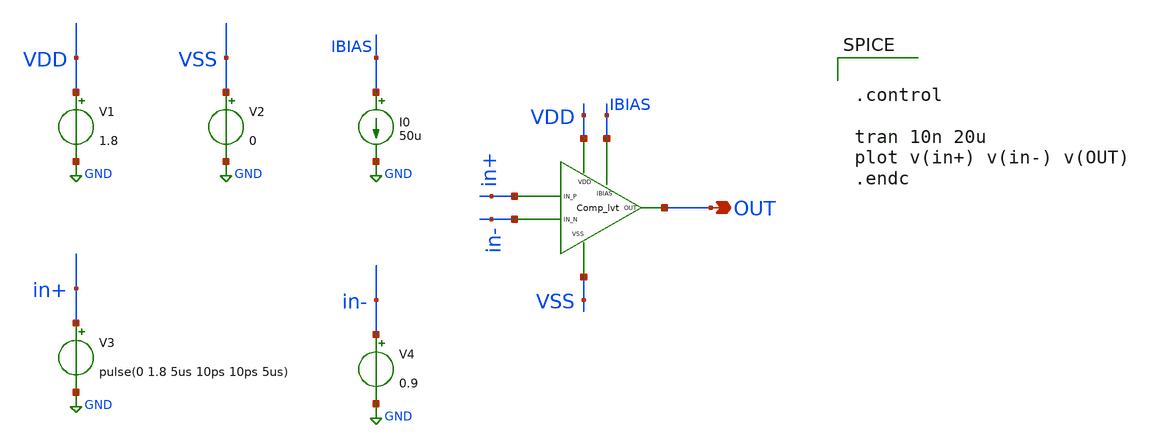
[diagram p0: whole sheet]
** sch_path: xschem/DC_DC_Converter_xschem/OTHERS/DC_DC_Converter_V7/Comparator/Comp_lvt_TB.sch
**.subckt Comp_lvt_TB OUT
*.opin OUT
XM1 IBIAS VDD in+ in- VSS OUT Comp_lvt
V1 VDD GND 1.8
V2 VSS GND 0
V3 in+ GND pulse(0 1.8 5us 10ps 10ps 5us)
V4 in- GND 0.9
I0 IBIAS GND 50u
**** begin user architecture code


.control

tran 10n 20u
plot v(in+) v(in-) v(OUT)
.endc



** opencircuitdesign pdks install
.lib $::SKYWATER_MODELS/sky130.lib.spice tt


**** end user architecture code
**.ends

* expanding   symbol:  DC_DC_Converter/Comparator/Comp_lvt.sym # of pins=6
** sym_path: xschem/DC_DC_Converter_xschem/OTHERS/DC_DC_Converter_V7/Comparator/Comp_lvt.sym
** sch_path: xschem/DC_DC_Converter_xschem/OTHERS/DC_DC_Converter_V7/Comparator/Comp_lvt.sch
.subckt Comp_lvt IBIAS VDD IN_P IN_N VSS OUT
*.iopin VSS
*.iopin VDD
*.iopin IN_P
*.iopin IN_N
*.iopin OUT
*.iopin IBIAS
XM16 2_P 1_N VDD VDD sky130_fd_pr__pfet_01v8_lvt L=0.5 W=3 nf=1 ad='int((nf+1)/2) * W/nf * 0.29' as='int((nf+2)/2) * W/nf * 0.29'
+ pd='2*int((nf+1)/2) * (W/nf + 0.29)' ps='2*int((nf+2)/2) * (W/nf + 0.29)' nrd='0.29 / W' nrs='0.29 / W'
+ sa=0 sb=0 sd=0 mult=1 m=1
XM4 1_N 1_N VDD VDD sky130_fd_pr__pfet_01v8_lvt L=0.5 W=3 nf=1 ad='int((nf+1)/2) * W/nf * 0.29' as='int((nf+2)/2) * W/nf * 0.29'
+ pd='2*int((nf+1)/2) * (W/nf + 0.29)' ps='2*int((nf+2)/2) * (W/nf + 0.29)' nrd='0.29 / W' nrs='0.29 / W'
+ sa=0 sb=0 sd=0 mult=1 m=1
XM5 1_N 1_P VDD VDD sky130_fd_pr__pfet_01v8_lvt L=0.5 W=3 nf=1 ad='int((nf+1)/2) * W/nf * 0.29' as='int((nf+2)/2) * W/nf * 0.29'
+ pd='2*int((nf+1)/2) * (W/nf + 0.29)' ps='2*int((nf+2)/2) * (W/nf + 0.29)' nrd='0.29 / W' nrs='0.29 / W'
+ sa=0 sb=0 sd=0 mult=1 m=1
XM3 1_P 1_N VDD VDD sky130_fd_pr__pfet_01v8_lvt L=0.5 W=3 nf=1 ad='int((nf+1)/2) * W/nf * 0.29' as='int((nf+2)/2) * W/nf * 0.29'
+ pd='2*int((nf+1)/2) * (W/nf + 0.29)' ps='2*int((nf+2)/2) * (W/nf + 0.29)' nrd='0.29 / W' nrs='0.29 / W'
+ sa=0 sb=0 sd=0 mult=1 m=1
XM6 1_P 1_P VDD VDD sky130_fd_pr__pfet_01v8_lvt L=0.5 W=3 nf=1 ad='int((nf+1)/2) * W/nf * 0.29' as='int((nf+2)/2) * W/nf * 0.29'
+ pd='2*int((nf+1)/2) * (W/nf + 0.29)' ps='2*int((nf+2)/2) * (W/nf + 0.29)' nrd='0.29 / W' nrs='0.29 / W'
+ sa=0 sb=0 sd=0 mult=1 m=1
XM7 2_N 1_P VDD VDD sky130_fd_pr__pfet_01v8_lvt L=0.5 W=3 nf=1 ad='int((nf+1)/2) * W/nf * 0.29' as='int((nf+2)/2) * W/nf * 0.29'
+ pd='2*int((nf+1)/2) * (W/nf + 0.29)' ps='2*int((nf+2)/2) * (W/nf + 0.29)' nrd='0.29 / W' nrs='0.29 / W'
+ sa=0 sb=0 sd=0 mult=1 m=1
XM8 2_P 2_P VSS VSS sky130_fd_pr__nfet_01v8_lvt L=1 W=1 nf=1 ad='int((nf+1)/2) * W/nf * 0.29' as='int((nf+2)/2) * W/nf * 0.29'
+ pd='2*int((nf+1)/2) * (W/nf + 0.29)' ps='2*int((nf+2)/2) * (W/nf + 0.29)' nrd='0.29 / W' nrs='0.29 / W'
+ sa=0 sb=0 sd=0 mult=1 m=1
XM2 2_N 2_P VSS VSS sky130_fd_pr__nfet_01v8_lvt L=1 W=1 nf=1 ad='int((nf+1)/2) * W/nf * 0.29' as='int((nf+2)/2) * W/nf * 0.29'
+ pd='2*int((nf+1)/2) * (W/nf + 0.29)' ps='2*int((nf+2)/2) * (W/nf + 0.29)' nrd='0.29 / W' nrs='0.29 / W'
+ sa=0 sb=0 sd=0 mult=1 m=1
XM9 1_P IN_N IBIAS VSS sky130_fd_pr__nfet_01v8_lvt L=0.7 W=5 nf=1 ad='int((nf+1)/2) * W/nf * 0.29' as='int((nf+2)/2) * W/nf * 0.29'
+ pd='2*int((nf+1)/2) * (W/nf + 0.29)' ps='2*int((nf+2)/2) * (W/nf + 0.29)' nrd='0.29 / W' nrs='0.29 / W'
+ sa=0 sb=0 sd=0 mult=1 m=1
XM1 1_N IN_P IBIAS VSS sky130_fd_pr__nfet_01v8_lvt L=0.7 W=5 nf=1 ad='int((nf+1)/2) * W/nf * 0.29' as='int((nf+2)/2) * W/nf * 0.29'
+ pd='2*int((nf+1)/2) * (W/nf + 0.29)' ps='2*int((nf+2)/2) * (W/nf + 0.29)' nrd='0.29 / W' nrs='0.29 / W'
+ sa=0 sb=0 sd=0 mult=1 m=1
XM10 OUT 2_N VDD VDD sky130_fd_pr__pfet_01v8_lvt L=0.5 W=2.5 nf=1 ad='int((nf+1)/2) * W/nf * 0.29' as='int((nf+2)/2) * W/nf * 0.29'
+ pd='2*int((nf+1)/2) * (W/nf + 0.29)' ps='2*int((nf+2)/2) * (W/nf + 0.29)' nrd='0.29 / W' nrs='0.29 / W'
+ sa=0 sb=0 sd=0 mult=1 m=1
XM13 OUT 2_N VSS VSS sky130_fd_pr__nfet_01v8_lvt L=0.5 W=1 nf=1 ad='int((nf+1)/2) * W/nf * 0.29' as='int((nf+2)/2) * W/nf * 0.29'
+ pd='2*int((nf+1)/2) * (W/nf + 0.29)' ps='2*int((nf+2)/2) * (W/nf + 0.29)' nrd='0.29 / W' nrs='0.29 / W'
+ sa=0 sb=0 sd=0 mult=1 m=1
.ends

.GLOBAL GND
.end
